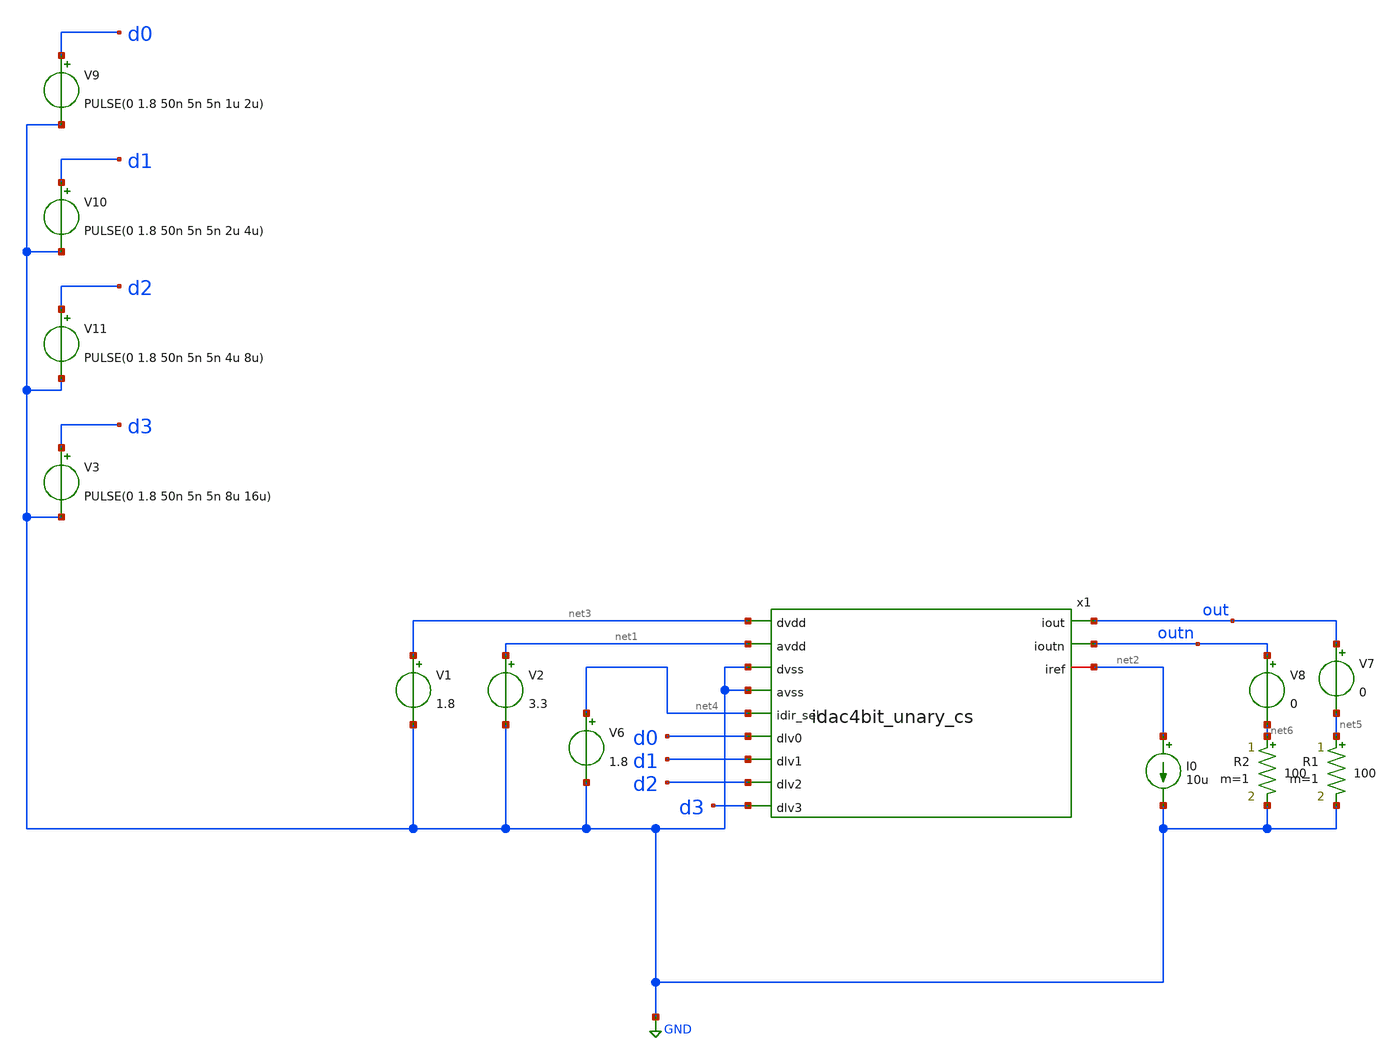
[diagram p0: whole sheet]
** sch_path: xschem/idac4bitthermo_cs_tb.sch
**.subckt idac4bitthermo_cs_tb
V1 net3 GND 1.8
V2 net1 GND 3.3
I0 net2 GND 10u
V3 d3 GND PULSE(0 1.8 50n 5n 5n 8u 16u)
V6 net4 GND 1.8
V7 out net5 0
R1 net5 GND 100 m=1
V8 outn net6 0
R2 net6 GND 100 m=1
V9 d0 GND PULSE(0 1.8 50n 5n 5n 1u 2u)
V10 d1 GND PULSE(0 1.8 50n 5n 5n 2u 4u)
V11 d2 GND PULSE(0 1.8 50n 5n 5n 4u 8u)
x1 out net3 net1 outn GND GND net4 d0 d1 d2 d3 net2 idac4bit_unary_cs
**** begin user architecture code
 .lib $::SKYWATER_MODELS/sky130.lib.spice tt
.include $::SKYWATER_STDCELLS/../../sky130_fd_sc_hvl/spice/sky130_fd_sc_hvl.spice

.param mc_mm_switch=0
.param mc_pr_switch=1



.option wnflag=0
.save v(out) v(outn)
.control
tran 200n 16u
plot v(out) v(outn)
write currentmirrortb.raw v(out) v(outn)
.endc


**** end user architecture code
**.ends
.GLOBAL GND
.end
